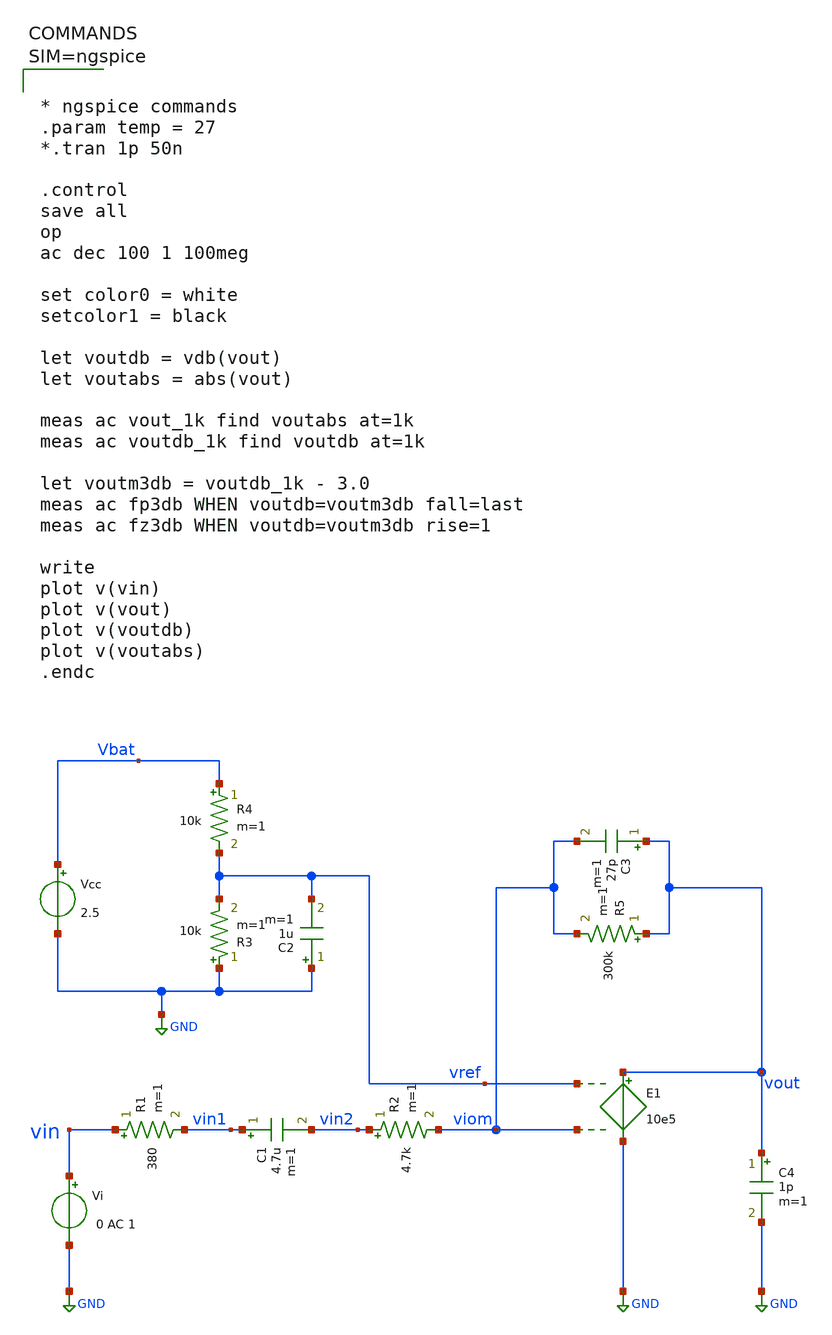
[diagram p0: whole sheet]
** sch_path: sch/MEMS_mic.sch
**.subckt MEMS_mic
R1 vin vin1 380 m=1
C1 vin1 vin2 4.7u m=1
R2 vin2 viom 4.7k m=1
E1 vout GND vref viom 10e5
Vi vin GND 0 AC 1
R3 GND vref 10k m=1
C2 GND vref 1u m=1
R4 Vbat vref 10k m=1
Vcc Vbat GND 2.5
R5 vout viom 300k m=1
C3 vout viom 27p m=1
C4 vout GND 1p m=1
**** begin user architecture code



* ngspice commands
.param temp = 27
*.tran 1p 50n

.control
save all
op
ac dec 100 1 100meg

set color0 = white
setcolor1 = black

let voutdb = vdb(vout)
let voutabs = abs(vout)

meas ac vout_1k find voutabs at=1k
meas ac voutdb_1k find voutdb at=1k

let voutm3db = voutdb_1k - 3.0
meas ac fp3db WHEN voutdb=voutm3db fall=last
meas ac fz3db WHEN voutdb=voutm3db rise=1

write
plot v(vin)
plot v(vout)
plot v(voutdb)
plot v(voutabs)
.endc



**** end user architecture code
**.ends
.GLOBAL GND
.end
